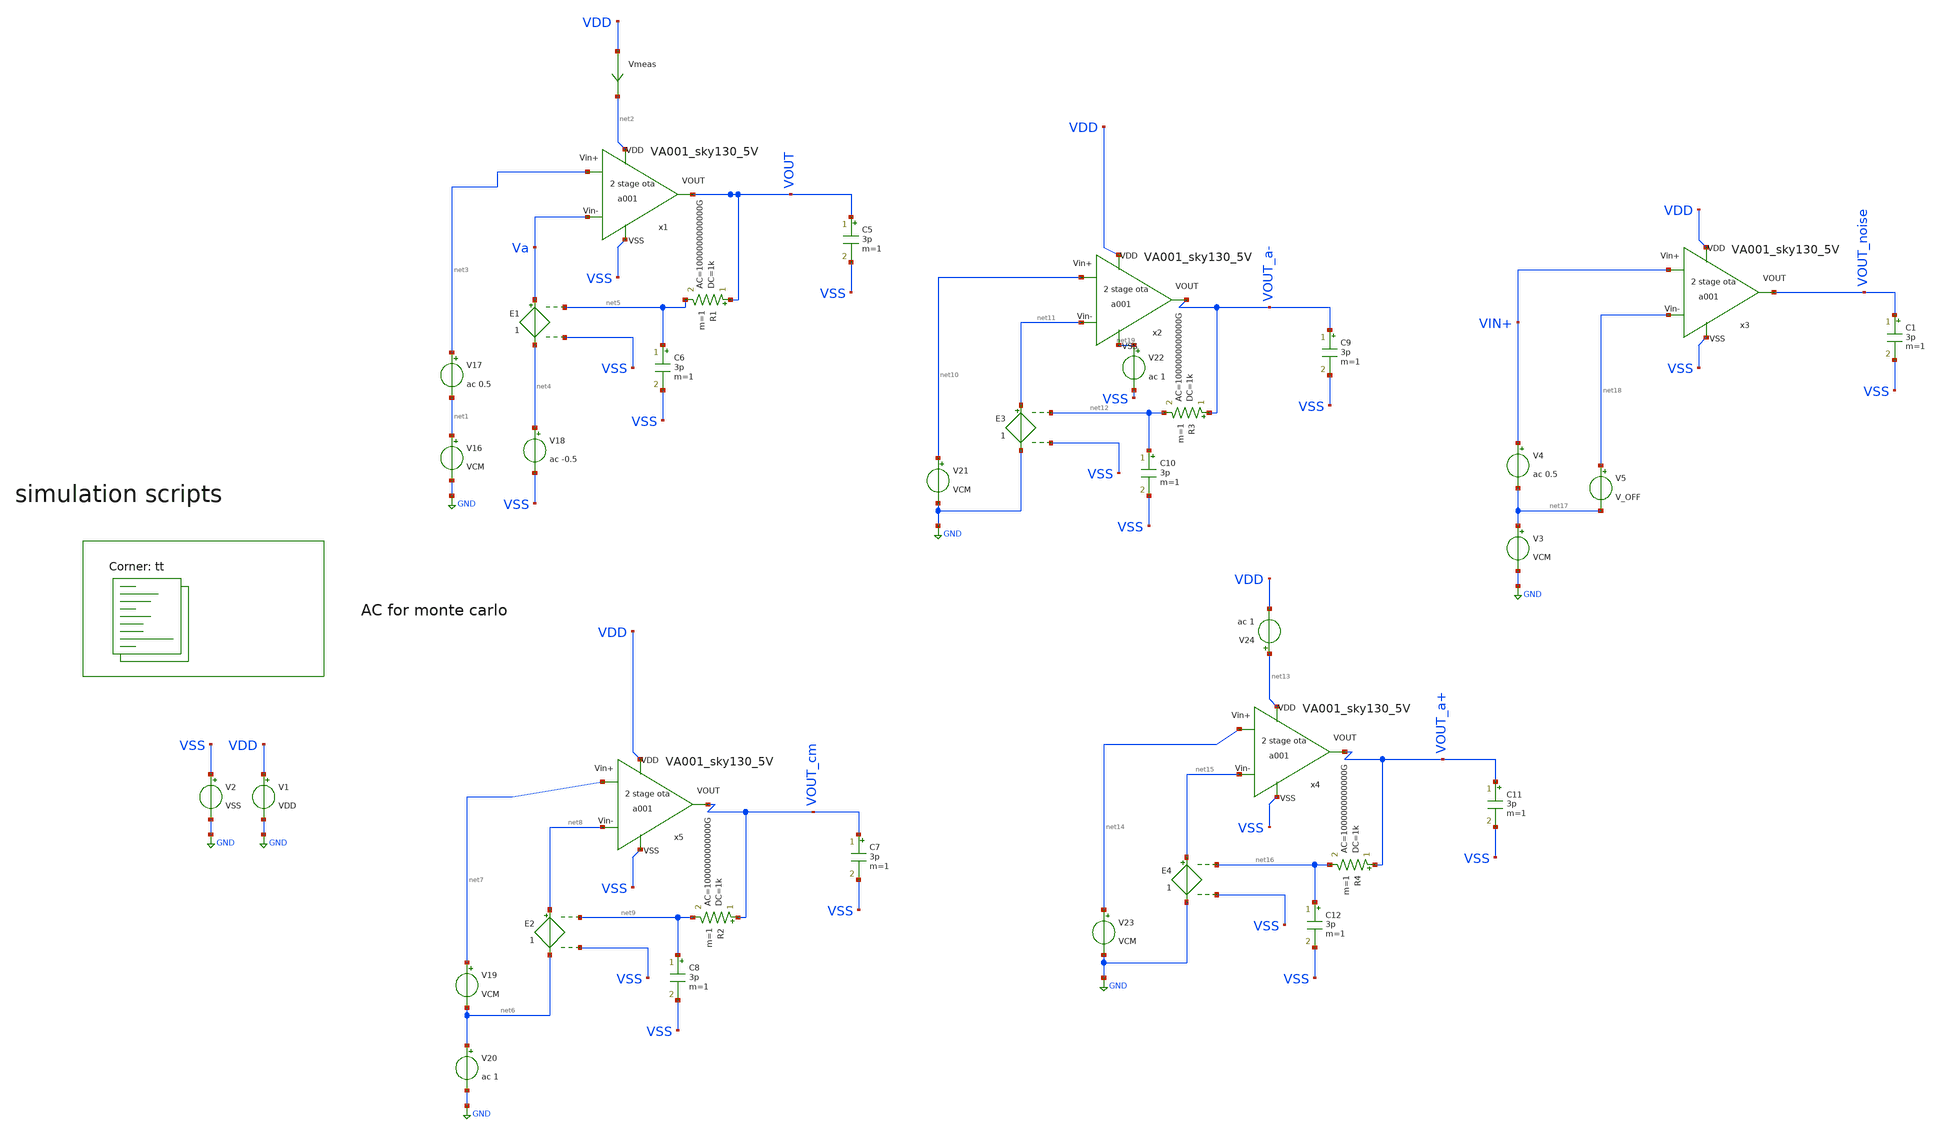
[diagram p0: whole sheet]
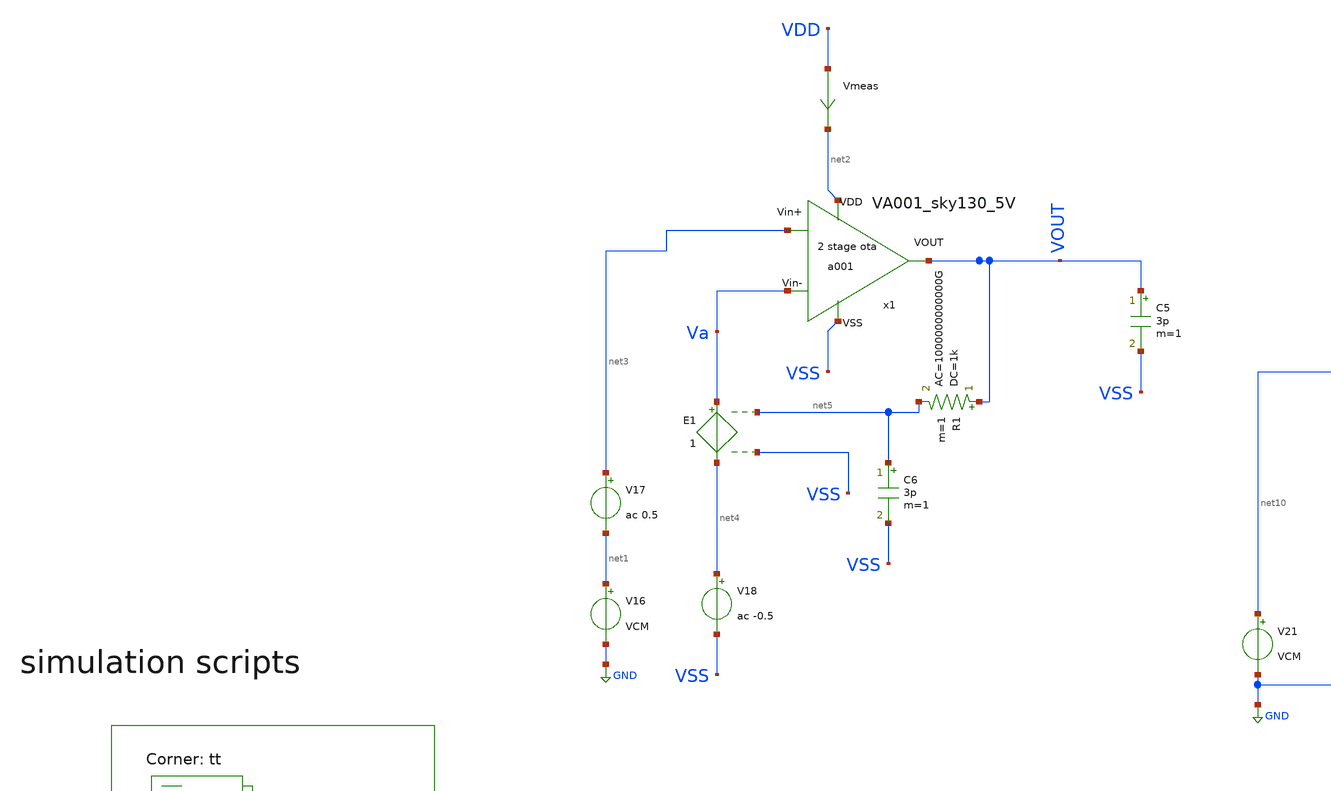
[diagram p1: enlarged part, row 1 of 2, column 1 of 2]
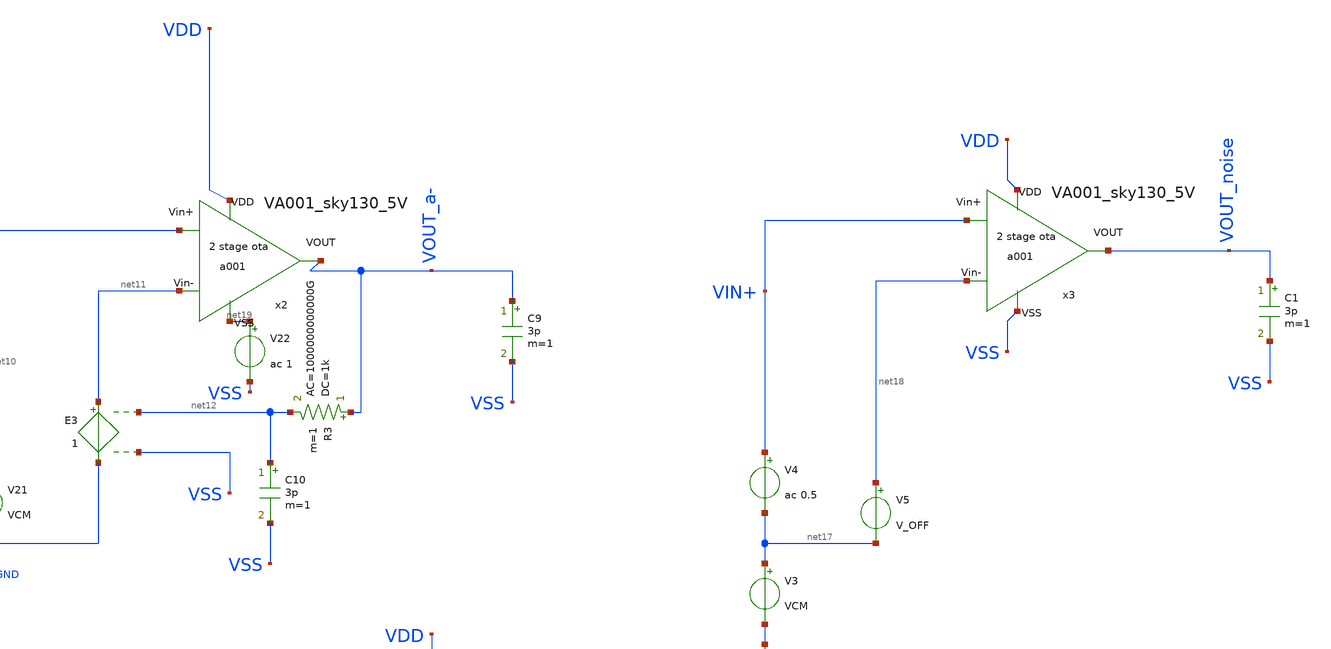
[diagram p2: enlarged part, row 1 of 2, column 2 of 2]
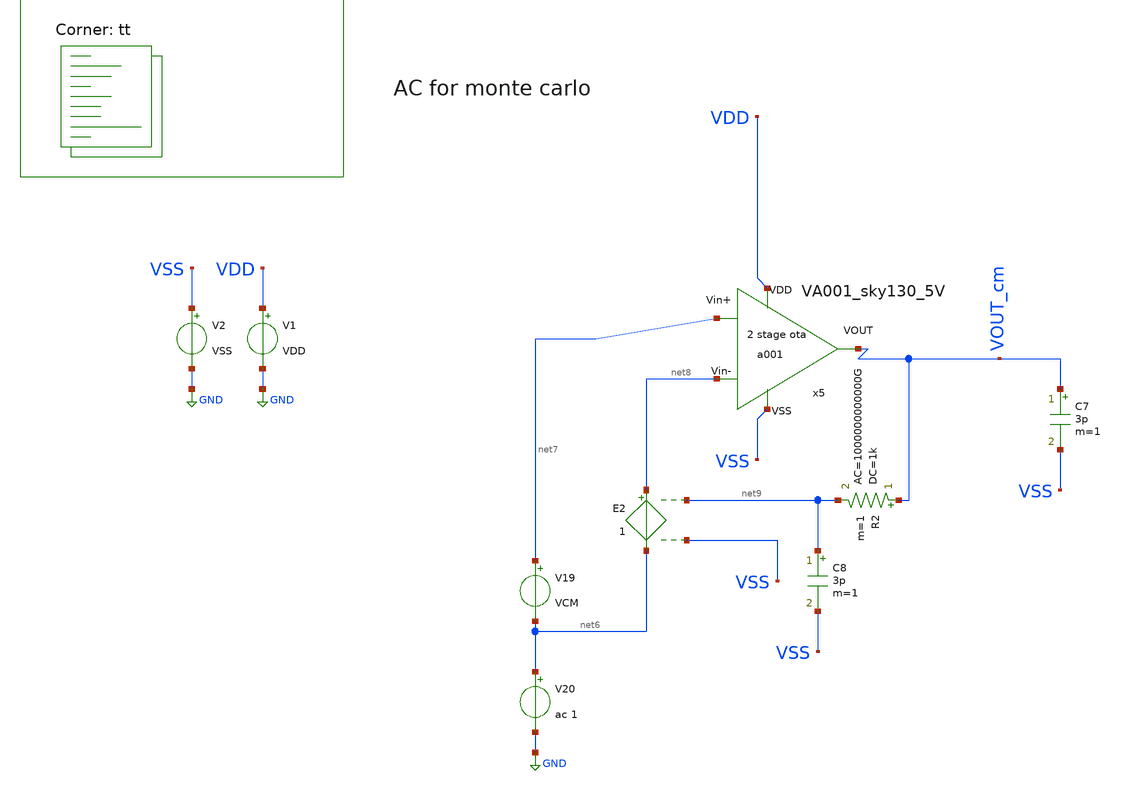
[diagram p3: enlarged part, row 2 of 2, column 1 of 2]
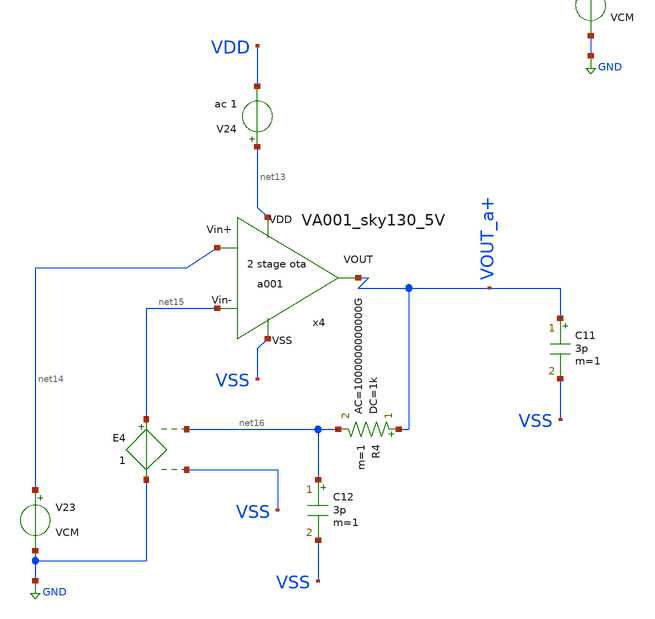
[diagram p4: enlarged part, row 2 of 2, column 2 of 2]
** sch_path: Learning/single_ended_amplifiers/VA001_series/Design_and_Analysis_of_Two-Stage_CMOS_Operational_Amplifier_for_Fluorescence_Signal_Processing_sky130_5V/amplifier_design/OTA_AC_TB.sch
**.subckt OTA_AC_TB
V1 VDD GND VDD
V2 VSS GND VSS
Vmeas VDD net2 0
.save i(vmeas)
C5 VOUT VSS 3p m=1
V16 net1 GND VCM
V17 net3 net1 ac 0.5
V18 net4 VSS ac -0.5
E1 Va net4 net5 VSS 1
R1 VOUT net5 1k ac=1000000000000G m=1
C6 net5 VSS 3p m=1
C7 VOUT_cm VSS 3p m=1
V19 net7 net6 VCM
V20 net6 GND ac 1
E2 net8 net6 net9 VSS 1
R2 VOUT_cm net9 1k ac=1000000000000G m=1
C8 net9 VSS 3p m=1
C9 VOUT_a- VSS 3p m=1
V21 net10 GND VCM
E3 net11 GND net12 VSS 1
R3 VOUT_a- net12 1k ac=1000000000000G m=1
C10 net12 VSS 3p m=1
V22 net19 VSS ac 1
C11 VOUT_a+ VSS 3p m=1
V23 net14 GND VCM
E4 net15 GND net16 VSS 1
R4 VOUT_a+ net16 1k ac=1000000000000G m=1
C12 net16 VSS 3p m=1
V24 net13 VDD ac 1
V3 net17 GND VCM
V4 VIN+ net17 ac 0.5
V5 net18 net17 V_OFF
C1 VOUT_noise VSS 3p m=1
x1 net2 VSS net3 Va VOUT VA001_sky130_5V
x2 VDD net19 net10 net11 VOUT_a- VA001_sky130_5V
x3 VDD VSS VIN+ net18 VOUT_noise VA001_sky130_5V
x4 net13 VSS net14 net15 VOUT_a+ VA001_sky130_5V
x5 VDD VSS net7 net8 VOUT_cm VA001_sky130_5V
**** begin user architecture code
.lib $::SKYWATER_MODELS/sky130.lib.spice tt

.Temp 27
.param VDD = 5
.param VSS = 0
.param CL = 3p
.param V_OFF = -400u
.param VCM=2.5


.control

	save all
	ac dec 100 1 10G
	plot db(v(VOUT)) (180+(180*ph(v(VOUT))/pi))
	plot (db(v(VOUT)) - db(v(VOUT_CM)))
	plot (db(v(VOUT)) - db(v(VOUT_A-)))
	plot (db(v(VOUT))- db(v(VOUT_A+)))
	wrdata VIN_sweep_AC.csv db(v(VOUT)) phase(v(VOUT)) db(v(VOUT_CM)) db(v(VOUT_A-)) db(v(VOUT_A+))

	noise v(VOUT_noise,VSS) V4 dec 10 1 40000k
	print inoise_total
	print onoise_total
	setplot noise1

	plot onoise_spectrum
	plot inoise_spectrum
	op
	print (2.5-V(VOUT))
	print v(VOUT_noise)

.endc




**** end user architecture code
**.ends

* expanding   symbol:  Sky130A/single ended amplifiers/VA001_sky130_5V.sym # of pins=5
** sym_path: LIB/Sky130A/single ended amplifiers/VA001_sky130_5V.sym
** sch_path: LIB/Sky130A/single ended amplifiers/VA001_sky130_5V.sch
.subckt VA001_sky130_5V VDD VSS Vin+ Vin- VOUT
*.iopin VDD
*.iopin VSS
*.iopin Vin+
*.iopin Vin-
*.iopin VOUT
XM9 VB1 VB2 net3 VSS sky130_fd_pr__nfet_g5v0d10v5 L=2 W='1 * 2 ' nf=2 ad='int((nf+1)/2) * W / nf * 0.29'
+ as='int((nf+2)/2) * W / nf * 0.29' pd='2*int((nf+1)/2) * (W / nf + 0.29)' ps='2*int((nf+2)/2) * (W / nf + 0.29)'
+ nrd='0.29 / W ' nrs='0.29 / W ' sa=0 sb=0 sd=0 mult=2 m=2
XM10 VB2 VB2 net1 VSS sky130_fd_pr__nfet_g5v0d10v5 L=2 W='1 * 2 ' nf=2 ad='int((nf+1)/2) * W / nf * 0.29'
+ as='int((nf+2)/2) * W / nf * 0.29' pd='2*int((nf+1)/2) * (W / nf + 0.29)' ps='2*int((nf+2)/2) * (W / nf + 0.29)'
+ nrd='0.29 / W ' nrs='0.29 / W ' sa=0 sb=0 sd=0 mult=2 m=2
XM3 VB2 VB1 VDD VDD sky130_fd_pr__pfet_g5v0d10v5 L=2.5 W='1 * 2 ' nf=2 ad='int((2 + 1)/2) * 1 * 0.29'
+ as='int((2 + 2)/2) * 1 * 0.29' pd='2*int((2 + 1)/2) * (1 + 0.29)' ps='2*int((2 + 2)/2) * (1 + 0.29)'
+ nrd='0.29 / 1 / 2 ' nrs='0.29 / 1 / 2 ' sa=0 sb=0 sd=0 mult=2 m=2
XM4 VB1 VB1 VDD VDD sky130_fd_pr__pfet_g5v0d10v5 L=2.5 W='1 * 2 ' nf=2 ad='int((2 + 1)/2) * 1 * 0.29'
+ as='int((2 + 2)/2) * 1 * 0.29' pd='2*int((2 + 1)/2) * (1 + 0.29)' ps='2*int((2 + 2)/2) * (1 + 0.29)'
+ nrd='0.29 / 1 / 2 ' nrs='0.29 / 1 / 2 ' sa=0 sb=0 sd=0 mult=2 m=2
XM5 net1 net1 VSS VSS sky130_fd_pr__nfet_g5v0d10v5 L=3 W='1.2 * 2 ' nf=2 ad='int((nf+1)/2) * W / nf * 0.29'
+ as='int((nf+2)/2) * W / nf * 0.29' pd='2*int((nf+1)/2) * (W / nf + 0.29)' ps='2*int((nf+2)/2) * (W / nf + 0.29)'
+ nrd='0.29 / W ' nrs='0.29 / W ' sa=0 sb=0 sd=0 mult=2 m=2
XM6 net3 net1 net2 VSS sky130_fd_pr__nfet_g5v0d10v5 L=3 W='1.2 * 2 ' nf=2 ad='int((nf+1)/2) * W / nf * 0.29'
+ as='int((nf+2)/2) * W / nf * 0.29' pd='2*int((nf+1)/2) * (W / nf + 0.29)' ps='2*int((nf+2)/2) * (W / nf + 0.29)'
+ nrd='0.29 / W ' nrs='0.29 / W ' sa=0 sb=0 sd=0 mult=8 m=8
XR2 VSS net2 VSS sky130_fd_pr__res_high_po_0p35 L=20 mult=1 m=1
XM1 net4 VB1 VDD VDD sky130_fd_pr__pfet_g5v0d10v5 L=2.5 W='1 * 2 ' nf=2 ad='int((2 + 1)/2) * 1 * 0.29'
+ as='int((2 + 2)/2) * 1 * 0.29' pd='2*int((2 + 1)/2) * (1 + 0.29)' ps='2*int((2 + 2)/2) * (1 + 0.29)'
+ nrd='0.29 / 1 / 2 ' nrs='0.29 / 1 / 2 ' sa=0 sb=0 sd=0 mult=6 m=6
XM2 net6 Vin- net4 net4 sky130_fd_pr__pfet_g5v0d10v5 L=1 W='3 * 2 ' nf=2 ad='int((2 + 1)/2) * 3 * 0.29'
+ as='int((2 + 2)/2) * 3 * 0.29' pd='2*int((2 + 1)/2) * (3 + 0.29)' ps='2*int((2 + 2)/2) * (3 + 0.29)'
+ nrd='0.29 / 3 / 2 ' nrs='0.29 / 3 / 2 ' sa=0 sb=0 sd=0 mult=4 m=4
XM11 net6 net6 VSS VSS sky130_fd_pr__nfet_g5v0d10v5 L=2 W='1.2 * 2 ' nf=2 ad='int((nf+1)/2) * W / nf * 0.29'
+ as='int((nf+2)/2) * W / nf * 0.29' pd='2*int((nf+1)/2) * (W / nf + 0.29)' ps='2*int((nf+2)/2) * (W / nf + 0.29)'
+ nrd='0.29 / W ' nrs='0.29 / W ' sa=0 sb=0 sd=0 mult=2 m=2
XM8 net5 net6 VSS VSS sky130_fd_pr__nfet_g5v0d10v5 L=2 W='1.2 * 2 ' nf=2 ad='int((nf+1)/2) * W / nf * 0.29'
+ as='int((nf+2)/2) * W / nf * 0.29' pd='2*int((nf+1)/2) * (W / nf + 0.29)' ps='2*int((nf+2)/2) * (W / nf + 0.29)'
+ nrd='0.29 / W ' nrs='0.29 / W ' sa=0 sb=0 sd=0 mult=2 m=2
XM12 VOUT net5 VSS VSS sky130_fd_pr__nfet_g5v0d10v5 L=1 W='2 * 4 ' nf=4 ad='int((nf+1)/2) * W / nf * 0.29'
+ as='int((nf+2)/2) * W / nf * 0.29' pd='2*int((nf+1)/2) * (W / nf + 0.29)' ps='2*int((nf+2)/2) * (W / nf + 0.29)'
+ nrd='0.29 / W ' nrs='0.29 / W ' sa=0 sb=0 sd=0 mult=2 m=2
XM7 net5 Vin+ net4 net4 sky130_fd_pr__pfet_g5v0d10v5 L=1 W='3 * 2 ' nf=2 ad='int((2 + 1)/2) * 3 * 0.29'
+ as='int((2 + 2)/2) * 3 * 0.29' pd='2*int((2 + 1)/2) * (3 + 0.29)' ps='2*int((2 + 2)/2) * (3 + 0.29)'
+ nrd='0.29 / 3 / 2 ' nrs='0.29 / 3 / 2 ' sa=0 sb=0 sd=0 mult=4 m=4
XM13 VOUT VB1 VDD VDD sky130_fd_pr__pfet_g5v0d10v5 L=2.5 W='1 * 2 ' nf=2 ad='int((2 + 1)/2) * 1 * 0.29'
+ as='int((2 + 2)/2) * 1 * 0.29' pd='2*int((2 + 1)/2) * (1 + 0.29)' ps='2*int((2 + 2)/2) * (1 + 0.29)'
+ nrd='0.29 / 1 / 2 ' nrs='0.29 / 1 / 2 ' sa=0 sb=0 sd=0 mult=14 m=14
XM14 net7 VB2 net5 VSS sky130_fd_pr__nfet_g5v0d10v5 L=2.1 W='1.2 * 2 ' nf=2 ad='int((nf+1)/2) * W / nf * 0.29'
+ as='int((nf+2)/2) * W / nf * 0.29' pd='2*int((nf+1)/2) * (W / nf + 0.29)' ps='2*int((nf+2)/2) * (W / nf + 0.29)'
+ nrd='0.29 / W ' nrs='0.29 / W ' sa=0 sb=0 sd=0 mult=1 m=1
XC1 net7 VOUT sky130_fd_pr__cap_mim_m3_1 W=7.5 L=7.5 MF=4 m=4
.ends

.GLOBAL GND
.end
